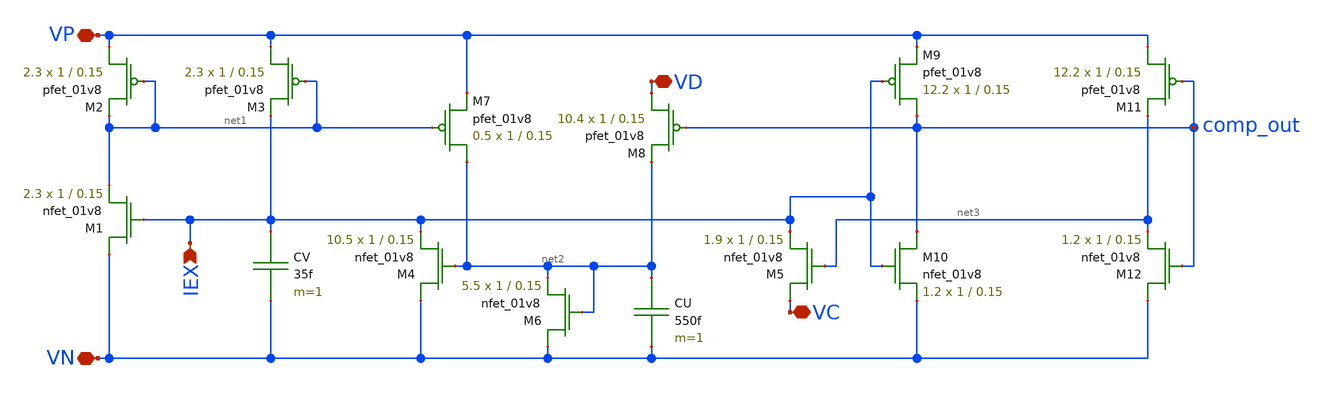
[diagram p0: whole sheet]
** sch_path: schematic/ronchini_neuron.sch
**.subckt ronchini_neuron VN VP IEX VD VC
*.iopin VN
*.iopin VP
*.ipin IEX
*.iopin VD
*.iopin VC
CV IEX VN 35f m=1
CU net2 VN 550f m=1
XM7 net2 net1 VP VDD sky130_fd_pr__pfet_01v8 L=0.15 W=1 nf=1 ad='int((nf+1)/2) * W/nf * 0.29' as='int((nf+2)/2) * W/nf * 0.29'
+ pd='2*int((nf+1)/2) * (W/nf + 0.29)' ps='2*int((nf+2)/2) * (W/nf + 0.29)' nrd='0.29 / W' nrs='0.29 / W'
+ sa=0 sb=0 sd=0 mult=0.5 m=0.5
XM8 VD comp_out net2 VDD sky130_fd_pr__pfet_01v8 L=0.15 W=1 nf=1 ad='int((nf+1)/2) * W/nf * 0.29' as='int((nf+2)/2) * W/nf * 0.29'
+ pd='2*int((nf+1)/2) * (W/nf + 0.29)' ps='2*int((nf+2)/2) * (W/nf + 0.29)' nrd='0.29 / W' nrs='0.29 / W'
+ sa=0 sb=0 sd=0 mult=10.4 m=10.4
XM10 comp_out IEX VN GND sky130_fd_pr__nfet_01v8 L=0.15 W=1 nf=1 ad='int((nf+1)/2) * W/nf * 0.29' as='int((nf+2)/2) * W/nf * 0.29'
+ pd='2*int((nf+1)/2) * (W/nf + 0.29)' ps='2*int((nf+2)/2) * (W/nf + 0.29)' nrd='0.29 / W' nrs='0.29 / W'
+ sa=0 sb=0 sd=0 mult=1.2 m=1.2
XM12 VN comp_out net3 GND sky130_fd_pr__nfet_01v8 L=0.15 W=1 nf=1 ad='int((nf+1)/2) * W/nf * 0.29' as='int((nf+2)/2) * W/nf * 0.29'
+ pd='2*int((nf+1)/2) * (W/nf + 0.29)' ps='2*int((nf+2)/2) * (W/nf + 0.29)' nrd='0.29 / W' nrs='0.29 / W'
+ sa=0 sb=0 sd=0 mult=1.2 m=1.2
XM5 VC net3 IEX GND sky130_fd_pr__nfet_01v8 L=0.15 W=1 nf=1 ad='int((nf+1)/2) * W/nf * 0.29' as='int((nf+2)/2) * W/nf * 0.29'
+ pd='2*int((nf+1)/2) * (W/nf + 0.29)' ps='2*int((nf+2)/2) * (W/nf + 0.29)' nrd='0.29 / W' nrs='0.29 / W'
+ sa=0 sb=0 sd=0 mult=1.9 m=1.9
XM2 VP net1 net1 VDD sky130_fd_pr__pfet_01v8 L=0.15 W=1 nf=1 ad='int((nf+1)/2) * W/nf * 0.29' as='int((nf+2)/2) * W/nf * 0.29'
+ pd='2*int((nf+1)/2) * (W/nf + 0.29)' ps='2*int((nf+2)/2) * (W/nf + 0.29)' nrd='0.29 / W' nrs='0.29 / W'
+ sa=0 sb=0 sd=0 mult=2.3 m=2.3
XM3 VP net1 IEX VDD sky130_fd_pr__pfet_01v8 L=0.15 W=1 nf=1 ad='int((nf+1)/2) * W/nf * 0.29' as='int((nf+2)/2) * W/nf * 0.29'
+ pd='2*int((nf+1)/2) * (W/nf + 0.29)' ps='2*int((nf+2)/2) * (W/nf + 0.29)' nrd='0.29 / W' nrs='0.29 / W'
+ sa=0 sb=0 sd=0 mult=2.3 m=2.3
XM1 VN IEX net1 GND sky130_fd_pr__nfet_01v8 L=0.15 W=1 nf=1 ad='int((nf+1)/2) * W/nf * 0.29' as='int((nf+2)/2) * W/nf * 0.29'
+ pd='2*int((nf+1)/2) * (W/nf + 0.29)' ps='2*int((nf+2)/2) * (W/nf + 0.29)' nrd='0.29 / W' nrs='0.29 / W'
+ sa=0 sb=0 sd=0 mult=2.3 m=2.3
XM4 VN net2 IEX GND sky130_fd_pr__nfet_01v8 L=0.15 W=1 nf=1 ad='int((nf+1)/2) * W/nf * 0.29' as='int((nf+2)/2) * W/nf * 0.29'
+ pd='2*int((nf+1)/2) * (W/nf + 0.29)' ps='2*int((nf+2)/2) * (W/nf + 0.29)' nrd='0.29 / W' nrs='0.29 / W'
+ sa=0 sb=0 sd=0 mult=10.5 m=10.5
XM6 VN net2 net2 GND sky130_fd_pr__nfet_01v8 L=0.15 W=1 nf=1 ad='int((nf+1)/2) * W/nf * 0.29' as='int((nf+2)/2) * W/nf * 0.29'
+ pd='2*int((nf+1)/2) * (W/nf + 0.29)' ps='2*int((nf+2)/2) * (W/nf + 0.29)' nrd='0.29 / W' nrs='0.29 / W'
+ sa=0 sb=0 sd=0 mult=5.5 m=5.5
XM9 comp_out IEX VP VDD sky130_fd_pr__pfet_01v8 L=0.15 W=1 nf=1 ad='int((nf+1)/2) * W/nf * 0.29' as='int((nf+2)/2) * W/nf * 0.29'
+ pd='2*int((nf+1)/2) * (W/nf + 0.29)' ps='2*int((nf+2)/2) * (W/nf + 0.29)' nrd='0.29 / W' nrs='0.29 / W'
+ sa=0 sb=0 sd=0 mult=12.2 m=12.2
XM11 VP comp_out net3 VDD sky130_fd_pr__pfet_01v8 L=0.15 W=1 nf=1 ad='int((nf+1)/2) * W/nf * 0.29' as='int((nf+2)/2) * W/nf * 0.29'
+ pd='2*int((nf+1)/2) * (W/nf + 0.29)' ps='2*int((nf+2)/2) * (W/nf + 0.29)' nrd='0.29 / W' nrs='0.29 / W'
+ sa=0 sb=0 sd=0 mult=12.2 m=12.2
**.ends
.end
